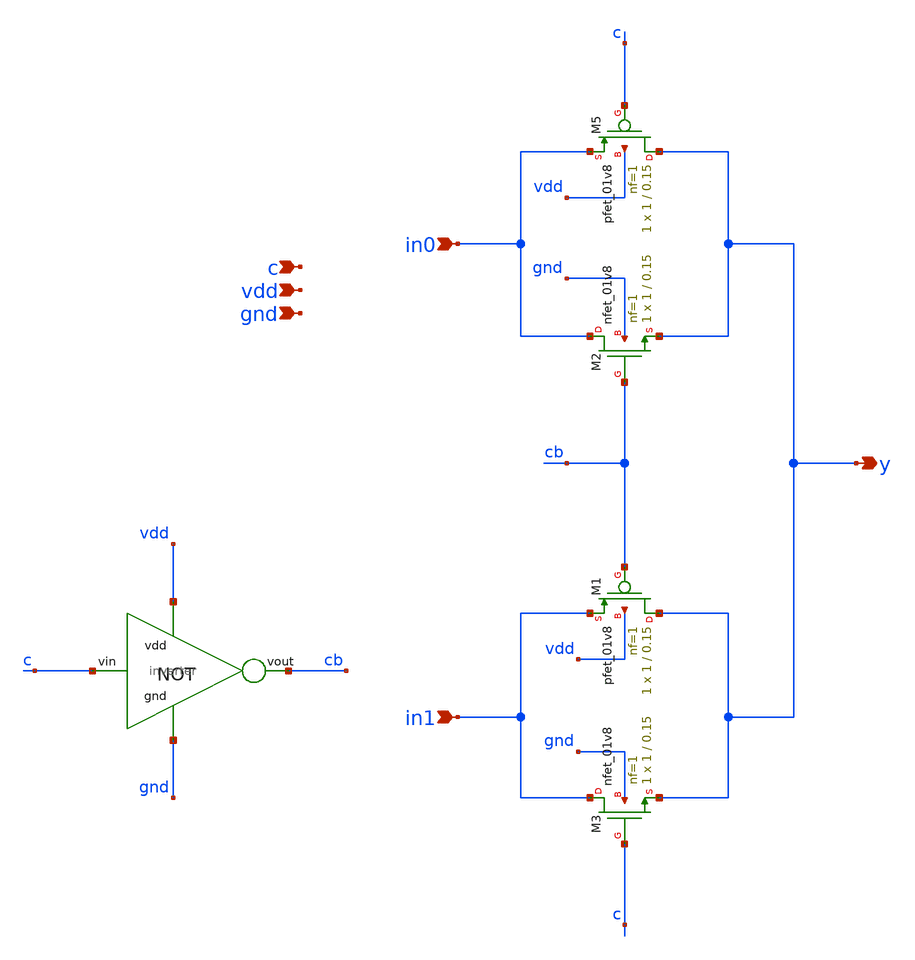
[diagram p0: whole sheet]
** sch_path: sram/mux2_tg.sch
**.subckt mux2_tg in0 in1 c y vdd gnd
*.ipin in0
*.ipin in1
*.ipin c
*.opin y
*.ipin vdd
*.ipin gnd
XM5 y c in0 vdd sky130_fd_pr__pfet_01v8 L=0.15 W=1 nf=1 ad='int((nf+1)/2) * W/nf * 0.29' as='int((nf+2)/2) * W/nf * 0.29'
+ pd='2*int((nf+1)/2) * (W/nf + 0.29)' ps='2*int((nf+2)/2) * (W/nf + 0.29)' nrd='0.29 / W' nrs='0.29 / W'
+ sa=0 sb=0 sd=0 mult=1 m=1
XM2 in0 cb y gnd sky130_fd_pr__nfet_01v8 L=0.15 W=1 nf=1 ad='int((nf+1)/2) * W/nf * 0.29' as='int((nf+2)/2) * W/nf * 0.29'
+ pd='2*int((nf+1)/2) * (W/nf + 0.29)' ps='2*int((nf+2)/2) * (W/nf + 0.29)' nrd='0.29 / W' nrs='0.29 / W'
+ sa=0 sb=0 sd=0 mult=1 m=1
XM1 y cb in1 vdd sky130_fd_pr__pfet_01v8 L=0.15 W=1 nf=1 ad='int((nf+1)/2) * W/nf * 0.29' as='int((nf+2)/2) * W/nf * 0.29'
+ pd='2*int((nf+1)/2) * (W/nf + 0.29)' ps='2*int((nf+2)/2) * (W/nf + 0.29)' nrd='0.29 / W' nrs='0.29 / W'
+ sa=0 sb=0 sd=0 mult=1 m=1
XM3 in1 c y gnd sky130_fd_pr__nfet_01v8 L=0.15 W=1 nf=1 ad='int((nf+1)/2) * W/nf * 0.29' as='int((nf+2)/2) * W/nf * 0.29'
+ pd='2*int((nf+1)/2) * (W/nf + 0.29)' ps='2*int((nf+2)/2) * (W/nf + 0.29)' nrd='0.29 / W' nrs='0.29 / W'
+ sa=0 sb=0 sd=0 mult=1 m=1
x1 vdd c cb gnd inverter
**.ends

* expanding   symbol:  inverter.sym # of pins=4
** sym_path: sram/inverter.sym
** sch_path: sram/inverter.sch
.subckt inverter vdd vin vout gnd
*.ipin vin
*.ipin vdd
*.ipin gnd
*.opin vout
XM1 vout vin gnd gnd sky130_fd_pr__nfet_01v8 L=0.15 W=1 nf=1 ad='int((nf+1)/2) * W/nf * 0.29' as='int((nf+2)/2) * W/nf * 0.29'
+ pd='2*int((nf+1)/2) * (W/nf + 0.29)' ps='2*int((nf+2)/2) * (W/nf + 0.29)' nrd='0.29 / W' nrs='0.29 / W'
+ sa=0 sb=0 sd=0 mult=1 m=1
XM2 vout vin vdd vdd sky130_fd_pr__pfet_01v8 L=0.15 W=1 nf=1 ad='int((nf+1)/2) * W/nf * 0.29' as='int((nf+2)/2) * W/nf * 0.29'
+ pd='2*int((nf+1)/2) * (W/nf + 0.29)' ps='2*int((nf+2)/2) * (W/nf + 0.29)' nrd='0.29 / W' nrs='0.29 / W'
+ sa=0 sb=0 sd=0 mult=1 m=1
.ends

.end
